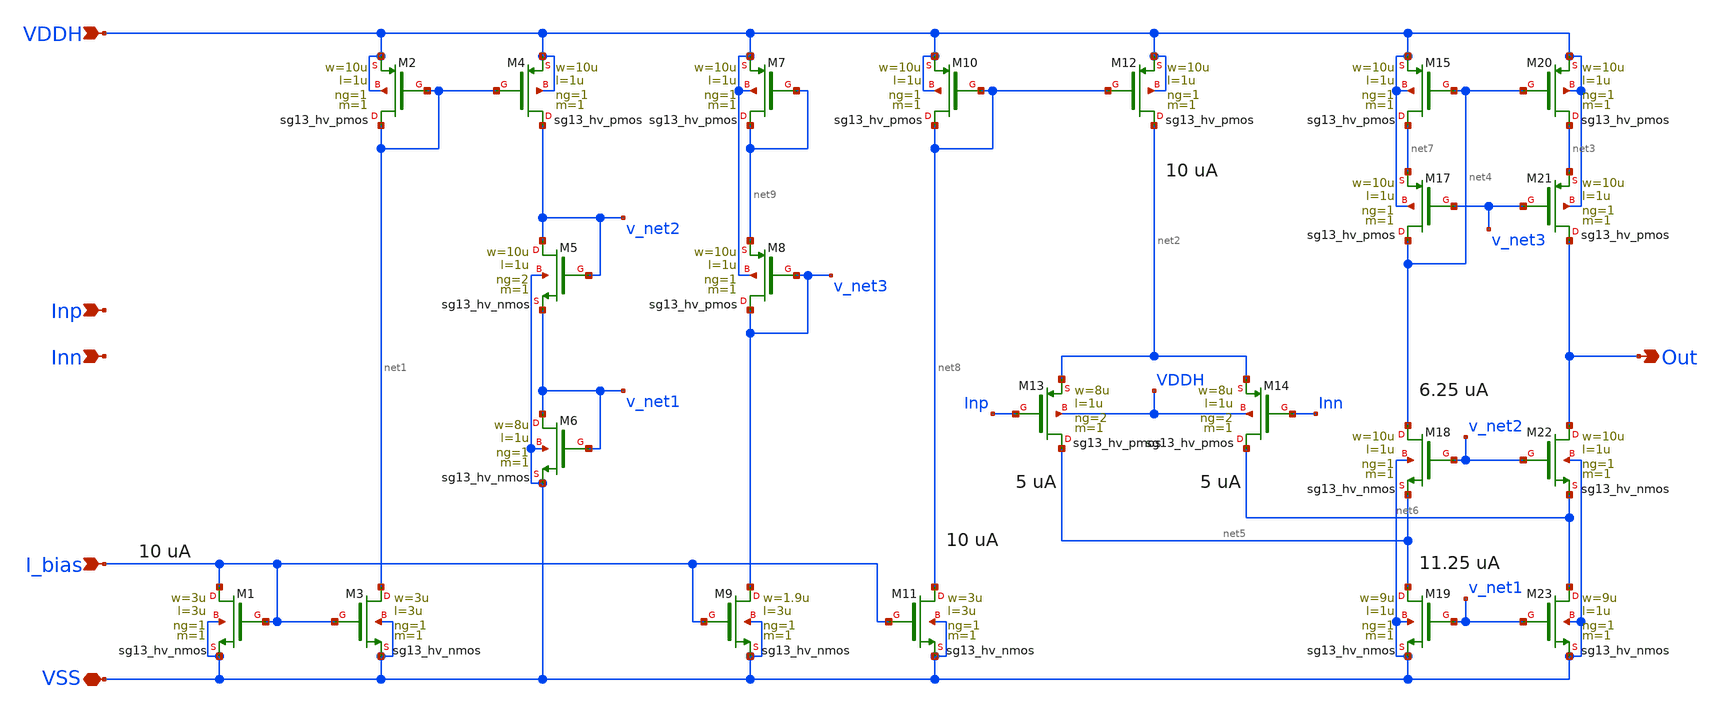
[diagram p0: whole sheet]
** sch_path: sar_adc/xschem/blocks/cascode_ota/ota_3.3v.sch
**.subckt ota_3.3v VDDH VSS I_bias Out Inp Inn
*.ipin VDDH
*.iopin VSS
*.ipin I_bias
*.opin Out
*.ipin Inp
*.ipin Inn
XM2 net1 net1 VDDH VDDH sg13_hv_pmos w=10u l=1u ng=1 m=1 mm_ok=1
XM3 net1 I_bias VSS VSS sg13_hv_nmos w=3u l=3u ng=1 m=1 mm_ok=1
XM1 I_bias I_bias VSS VSS sg13_hv_nmos w=3u l=3u ng=1 m=1 mm_ok=1
XM11 net8 I_bias VSS VSS sg13_hv_nmos w=3u l=3u ng=1 m=1 mm_ok=1
XM13 net5 Inp net2 VDDH sg13_hv_pmos w=8u l=1u ng=2 m=1 mm_ok=1
XM14 net6 Inn net2 VDDH sg13_hv_pmos w=8u l=1u ng=2 m=1 mm_ok=1
XM15 net7 net4 VDDH VDDH sg13_hv_pmos w=10u l=1u ng=1 m=1 mm_ok=1
XM20 net3 net4 VDDH VDDH sg13_hv_pmos w=10u l=1u ng=1 m=1 mm_ok=1
XM17 net4 v_net3 net7 VDDH sg13_hv_pmos w=10u l=1u ng=1 m=1 mm_ok=1
XM18 net4 v_net2 net5 VSS sg13_hv_nmos w=10u l=1u ng=1 m=1 mm_ok=1
XM19 net5 v_net1 VSS VSS sg13_hv_nmos w=9u l=1u ng=1 m=1 mm_ok=1
XM22 Out v_net2 net6 VSS sg13_hv_nmos w=10u l=1u ng=1 m=1 mm_ok=1
XM23 net6 v_net1 VSS VSS sg13_hv_nmos w=9u l=1u ng=1 m=1 mm_ok=1
XM12 net2 net8 VDDH VDDH sg13_hv_pmos w=10u l=1u ng=1 m=1 mm_ok=1
XM10 net8 net8 VDDH VDDH sg13_hv_pmos w=10u l=1u ng=1 m=1 mm_ok=1
XM6 v_net1 v_net1 VSS VSS sg13_hv_nmos w=8u l=1u ng=1 m=1 mm_ok=1
XM4 v_net2 net1 VDDH VDDH sg13_hv_pmos w=10u l=1u ng=1 m=1 mm_ok=1
XM5 v_net2 v_net2 v_net1 VSS sg13_hv_nmos w=10u l=1u ng=2 m=1 mm_ok=1
XM7 net9 net9 VDDH VDDH sg13_hv_pmos w=10u l=1u ng=1 m=1 mm_ok=1
XM9 v_net3 I_bias VSS VSS sg13_hv_nmos w=1.9u l=3u ng=1 m=1 mm_ok=1
XM8 v_net3 v_net3 net9 VDDH sg13_hv_pmos w=10u l=1u ng=1 m=1 mm_ok=1
XM21 Out v_net3 net3 VDDH sg13_hv_pmos w=10u l=1u ng=1 m=1 mm_ok=1
**.ends
.end
